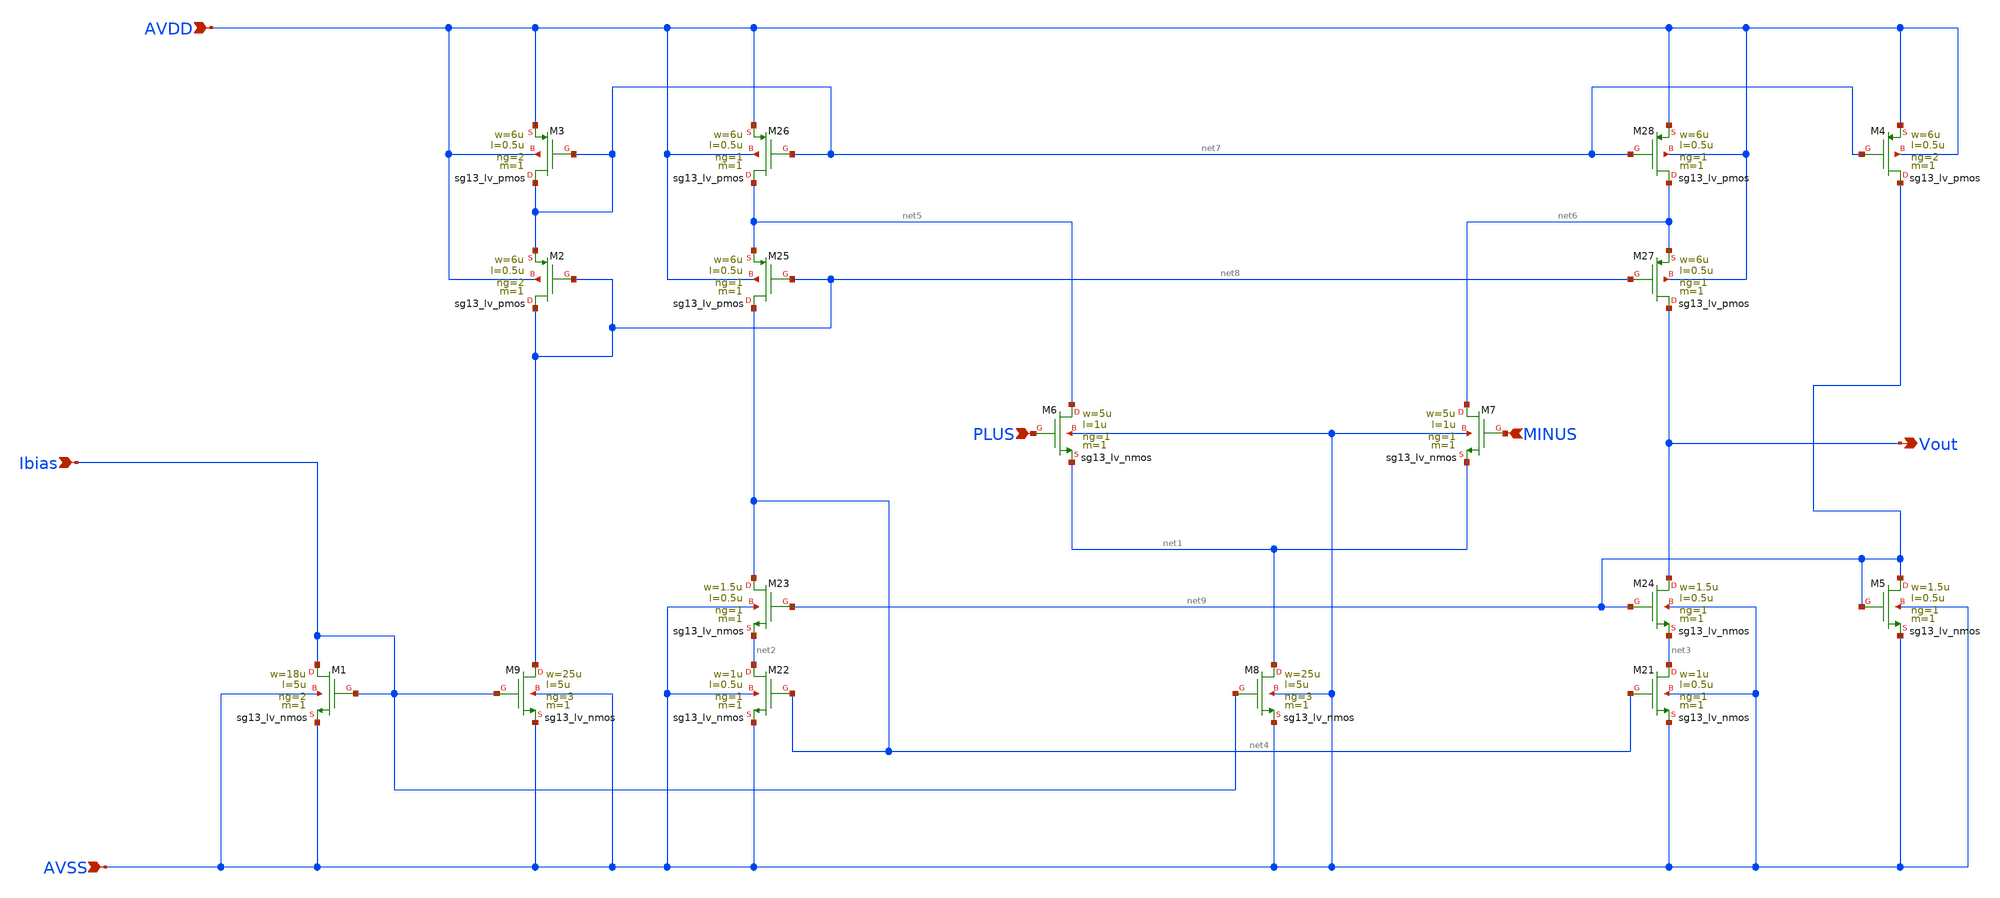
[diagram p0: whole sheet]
** sch_path: Designs/otas/foldedcascode_nmos.sch
**.subckt foldedcascode_nmos PLUS MINUS Vout AVDD AVSS Ibias
*.ipin PLUS
*.ipin MINUS
*.opin Vout
*.ipin AVDD
*.ipin AVSS
*.ipin Ibias
XM6 net5 PLUS net1 AVSS sg13_lv_nmos w=5u l=1u ng=1 m=1 mm_ok=1
XM8 net1 Ibias AVSS AVSS sg13_lv_nmos w=25u l=5u ng=3 m=1 mm_ok=1
XM21 net3 net4 AVSS AVSS sg13_lv_nmos w=1u l=0.5u ng=1 m=1 mm_ok=1
XM22 net2 net4 AVSS AVSS sg13_lv_nmos w=1u l=0.5u ng=1 m=1 mm_ok=1
XM7 net6 MINUS net1 AVSS sg13_lv_nmos w=5u l=1u ng=1 m=1 mm_ok=1
XM23 net4 net9 net2 AVSS sg13_lv_nmos w=1.5u l=0.5u ng=1 m=1 mm_ok=1
XM24 Vout net9 net3 AVSS sg13_lv_nmos w=1.5u l=0.5u ng=1 m=1 mm_ok=1
XM25 net4 net8 net5 AVDD sg13_lv_pmos w=6u l=0.5u ng=1 m=1 mm_ok=1
XM26 net5 net7 AVDD AVDD sg13_lv_pmos w=6u l=0.5u ng=1 m=1 mm_ok=1
XM27 Vout net8 net6 AVDD sg13_lv_pmos w=6u l=0.5u ng=1 m=1 mm_ok=1
XM28 net6 net7 AVDD AVDD sg13_lv_pmos w=6u l=0.5u ng=1 m=1 mm_ok=1
XM1 Ibias Ibias AVSS AVSS sg13_lv_nmos w=18u l=5u ng=2 m=1 mm_ok=1
XM2 net8 net8 net7 AVDD sg13_lv_pmos w=6u l=0.5u ng=2 m=1 mm_ok=1
XM3 net7 net7 AVDD AVDD sg13_lv_pmos w=6u l=0.5u ng=2 m=1 mm_ok=1
XM4 net9 net7 AVDD AVDD sg13_lv_pmos w=6u l=0.5u ng=2 m=1 mm_ok=1
XM5 net9 net9 AVSS AVSS sg13_lv_nmos w=1.5u l=0.5u ng=1 m=1 mm_ok=1
XM9 net8 Ibias AVSS AVSS sg13_lv_nmos w=25u l=5u ng=3 m=1 mm_ok=1
**.ends
.end
